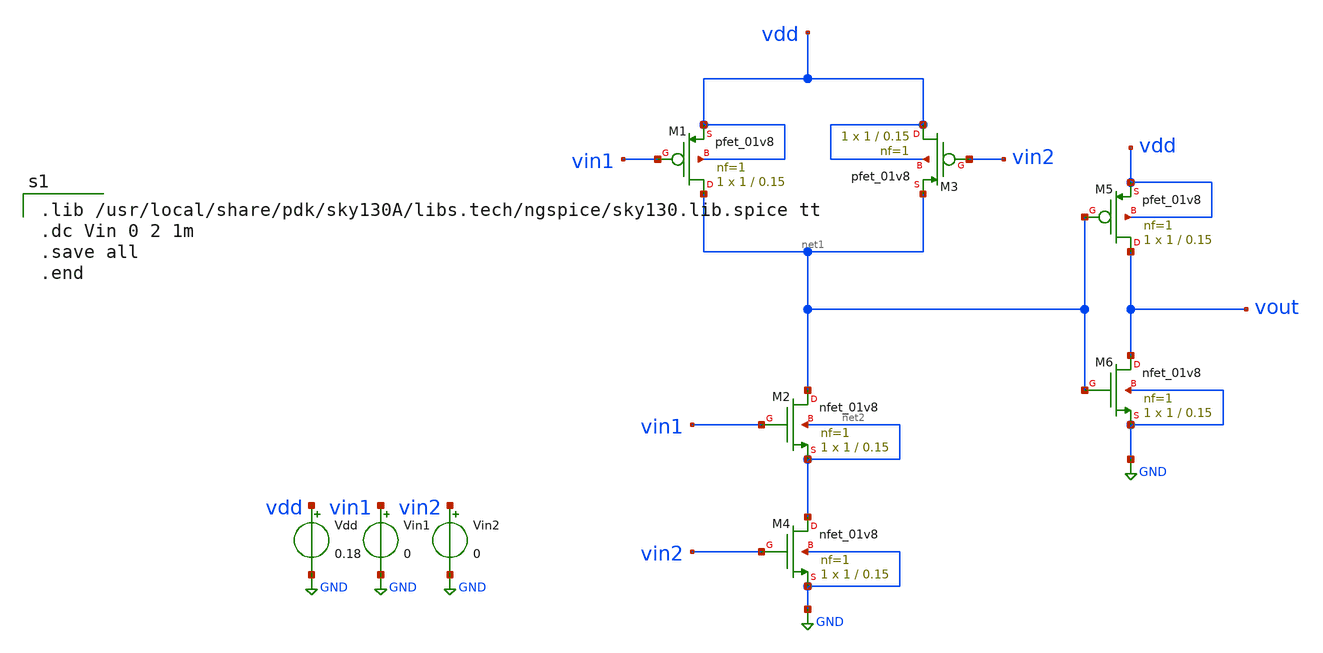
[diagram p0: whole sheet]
** sch_path: andgate.sch
**.subckt andgate
XM1 net1 vin1 vdd vdd sky130_fd_pr__pfet_01v8 L=0.15 W=1 nf=1 ad='int((1 + 1)/2) * 1 / 1 * 0.29' as='int((1 + 2)/2) * 1 / 1 * 0.29'
+ pd='2*int((1 + 1)/2) * (1 / 1 + 0.29)' ps='2*int((1 + 2)/2) * (1 / 1 + 0.29)' nrd='0.29 / 1 ' nrs='0.29 / 1 '
+ sa=0 sb=0 sd=0 mult=1 m=1
XM2 net1 vin1 net2 net2 sky130_fd_pr__nfet_01v8 L=0.15 W=1 nf=1 ad='int((1 + 1)/2) * 1 / 1 * 0.29' as='int((1 + 2)/2) * 1 / 1 * 0.29'
+ pd='2*int((1 + 1)/2) * (1 / 1 + 0.29)' ps='2*int((1 + 2)/2) * (1 / 1 + 0.29)' nrd='0.29 / 1 ' nrs='0.29 / 1 '
+ sa=0 sb=0 sd=0 mult=1 m=1
XM3 vdd vin2 net1 vdd sky130_fd_pr__pfet_01v8 L=0.15 W=1 nf=1 ad='int((1 + 1)/2) * 1 / 1 * 0.29' as='int((1 + 2)/2) * 1 / 1 * 0.29'
+ pd='2*int((1 + 1)/2) * (1 / 1 + 0.29)' ps='2*int((1 + 2)/2) * (1 / 1 + 0.29)' nrd='0.29 / 1 ' nrs='0.29 / 1 '
+ sa=0 sb=0 sd=0 mult=1 m=1
XM4 net2 vin2 GND GND sky130_fd_pr__nfet_01v8 L=0.15 W=1 nf=1 ad='int((1 + 1)/2) * 1 / 1 * 0.29' as='int((1 + 2)/2) * 1 / 1 * 0.29'
+ pd='2*int((1 + 1)/2) * (1 / 1 + 0.29)' ps='2*int((1 + 2)/2) * (1 / 1 + 0.29)' nrd='0.29 / 1 ' nrs='0.29 / 1 '
+ sa=0 sb=0 sd=0 mult=1 m=1
Vdd vdd GND 0.18
Vin1 vin1 GND 0
Vin2 vin2 GND 0
XM5 vout net1 vdd vdd sky130_fd_pr__pfet_01v8 L=0.15 W=1 nf=1 ad='int((1 + 1)/2) * 1 / 1 * 0.29' as='int((1 + 2)/2) * 1 / 1 * 0.29'
+ pd='2*int((1 + 1)/2) * (1 / 1 + 0.29)' ps='2*int((1 + 2)/2) * (1 / 1 + 0.29)' nrd='0.29 / 1 ' nrs='0.29 / 1 '
+ sa=0 sb=0 sd=0 mult=1 m=1
XM6 vout net1 GND GND sky130_fd_pr__nfet_01v8 L=0.15 W=1 nf=1 ad='int((1 + 1)/2) * 1 / 1 * 0.29' as='int((1 + 2)/2) * 1 / 1 * 0.29'
+ pd='2*int((1 + 1)/2) * (1 / 1 + 0.29)' ps='2*int((1 + 2)/2) * (1 / 1 + 0.29)' nrd='0.29 / 1 ' nrs='0.29 / 1 '
+ sa=0 sb=0 sd=0 mult=1 m=1
**** begin user architecture code

.lib /usr/local/share/pdk/sky130A/libs.tech/ngspice/sky130.lib.spice tt
.dc Vin 0 2 1m
.save all
.end

**** end user architecture code
**.ends
.GLOBAL GND
.end
